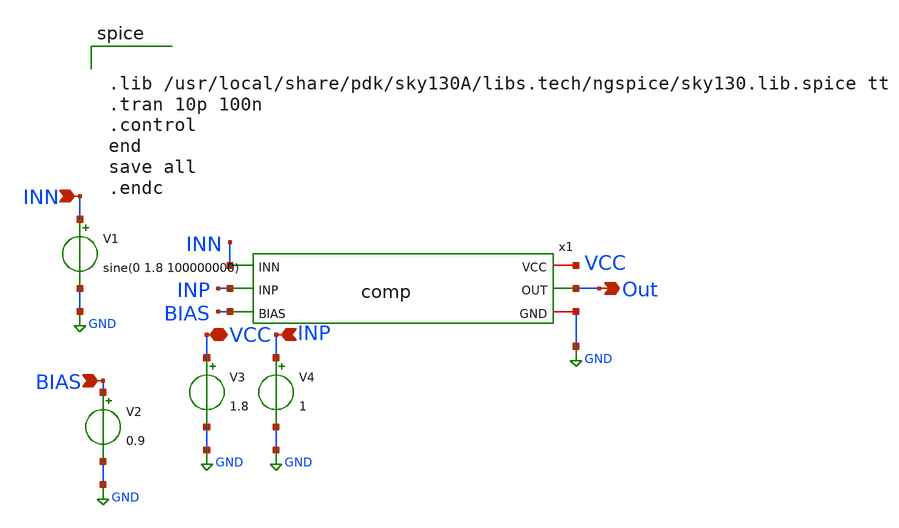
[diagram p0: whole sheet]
** sch_path: week7/pre-layout/tb_comp.sch
**.subckt tb_comp VCC Out INP INN BIAS
*.iopin VCC
*.opin Out
*.ipin INP
*.ipin INN
*.ipin BIAS
x1 VCC Out INN INP GND BIAS comp
V1 INN GND sine(0 1.8 100000000)
V2 BIAS GND 0.9
V3 VCC GND 1.8
V4 INP GND 1
**** begin user architecture code


.lib /usr/local/share/pdk/sky130A/libs.tech/ngspice/sky130.lib.spice tt
.tran 10p 100n
.control
end
save all
.endc


**** end user architecture code
**.ends

* expanding   symbol:  comp.sym # of pins=6
** sym_path: week7/pre-layout/comp.sym
** sch_path: week7/pre-layout/comp.sch
.subckt comp VCC OUT INN INP GND BIAS
*.ipin BIAS
*.iopin VCC
*.iopin GND
*.opin OUT
*.ipin INN
*.ipin INP
XM1 net3 net3 VCC VCC sky130_fd_pr__pfet_01v8 L=0.15 W=0.84 nf=1 ad='int((nf+1)/2) * W/nf * 0.29' as='int((nf+2)/2) * W/nf * 0.29'
+ pd='2*int((nf+1)/2) * (W/nf + 0.29)' ps='2*int((nf+2)/2) * (W/nf + 0.29)' nrd='0.29 / W' nrs='0.29 / W'
+ sa=0 sb=0 sd=0 mult=1 m=1
XM3 net3 INN net1 GND sky130_fd_pr__nfet_01v8 L=0.15 W=0.84 nf=1 ad='int((nf+1)/2) * W/nf * 0.29' as='int((nf+2)/2) * W/nf * 0.29'
+ pd='2*int((nf+1)/2) * (W/nf + 0.29)' ps='2*int((nf+2)/2) * (W/nf + 0.29)' nrd='0.29 / W' nrs='0.29 / W'
+ sa=0 sb=0 sd=0 mult=1 m=1
XM12 net1 BIAS GND GND sky130_fd_pr__nfet_01v8 L=0.15 W=0.84 nf=1 ad='int((nf+1)/2) * W/nf * 0.29' as='int((nf+2)/2) * W/nf * 0.29'
+ pd='2*int((nf+1)/2) * (W/nf + 0.29)' ps='2*int((nf+2)/2) * (W/nf + 0.29)' nrd='0.29 / W' nrs='0.29 / W'
+ sa=0 sb=0 sd=0 mult=1 m=1
XM2 net2 net3 VCC VCC sky130_fd_pr__pfet_01v8 L=0.15 W=0.84 nf=1 ad='int((nf+1)/2) * W/nf * 0.29' as='int((nf+2)/2) * W/nf * 0.29'
+ pd='2*int((nf+1)/2) * (W/nf + 0.29)' ps='2*int((nf+2)/2) * (W/nf + 0.29)' nrd='0.29 / W' nrs='0.29 / W'
+ sa=0 sb=0 sd=0 mult=1 m=1
XM4 net2 INP net1 GND sky130_fd_pr__nfet_01v8 L=0.15 W=0.84 nf=1 ad='int((nf+1)/2) * W/nf * 0.29' as='int((nf+2)/2) * W/nf * 0.29'
+ pd='2*int((nf+1)/2) * (W/nf + 0.29)' ps='2*int((nf+2)/2) * (W/nf + 0.29)' nrd='0.29 / W' nrs='0.29 / W'
+ sa=0 sb=0 sd=0 mult=1 m=1
XM5 net4 net2 VCC VCC sky130_fd_pr__pfet_01v8 L=0.15 W=0.84 nf=1 ad='int((nf+1)/2) * W/nf * 0.29' as='int((nf+2)/2) * W/nf * 0.29'
+ pd='2*int((nf+1)/2) * (W/nf + 0.29)' ps='2*int((nf+2)/2) * (W/nf + 0.29)' nrd='0.29 / W' nrs='0.29 / W'
+ sa=0 sb=0 sd=0 mult=1 m=1
XM6 net4 net2 GND GND sky130_fd_pr__nfet_01v8 L=0.15 W=0.84 nf=1 ad='int((nf+1)/2) * W/nf * 0.29' as='int((nf+2)/2) * W/nf * 0.29'
+ pd='2*int((nf+1)/2) * (W/nf + 0.29)' ps='2*int((nf+2)/2) * (W/nf + 0.29)' nrd='0.29 / W' nrs='0.29 / W'
+ sa=0 sb=0 sd=0 mult=1 m=1
XM7 net5 net4 GND GND sky130_fd_pr__nfet_01v8 L=0.15 W=0.84 nf=1 ad='int((nf+1)/2) * W/nf * 0.29' as='int((nf+2)/2) * W/nf * 0.29'
+ pd='2*int((nf+1)/2) * (W/nf + 0.29)' ps='2*int((nf+2)/2) * (W/nf + 0.29)' nrd='0.29 / W' nrs='0.29 / W'
+ sa=0 sb=0 sd=0 mult=1 m=1
XM8 OUT net5 GND GND sky130_fd_pr__nfet_01v8 L=0.15 W=0.84 nf=1 ad='int((nf+1)/2) * W/nf * 0.29' as='int((nf+2)/2) * W/nf * 0.29'
+ pd='2*int((nf+1)/2) * (W/nf + 0.29)' ps='2*int((nf+2)/2) * (W/nf + 0.29)' nrd='0.29 / W' nrs='0.29 / W'
+ sa=0 sb=0 sd=0 mult=1 m=1
XM9 net5 net4 VCC VCC sky130_fd_pr__pfet_01v8 L=0.15 W=0.84 nf=1 ad='int((nf+1)/2) * W/nf * 0.29' as='int((nf+2)/2) * W/nf * 0.29'
+ pd='2*int((nf+1)/2) * (W/nf + 0.29)' ps='2*int((nf+2)/2) * (W/nf + 0.29)' nrd='0.29 / W' nrs='0.29 / W'
+ sa=0 sb=0 sd=0 mult=1 m=1
XM10 OUT net5 VCC VCC sky130_fd_pr__pfet_01v8 L=0.15 W=0.84 nf=1 ad='int((nf+1)/2) * W/nf * 0.29' as='int((nf+2)/2) * W/nf * 0.29'
+ pd='2*int((nf+1)/2) * (W/nf + 0.29)' ps='2*int((nf+2)/2) * (W/nf + 0.29)' nrd='0.29 / W' nrs='0.29 / W'
+ sa=0 sb=0 sd=0 mult=1 m=1
.ends

.GLOBAL GND
.end
